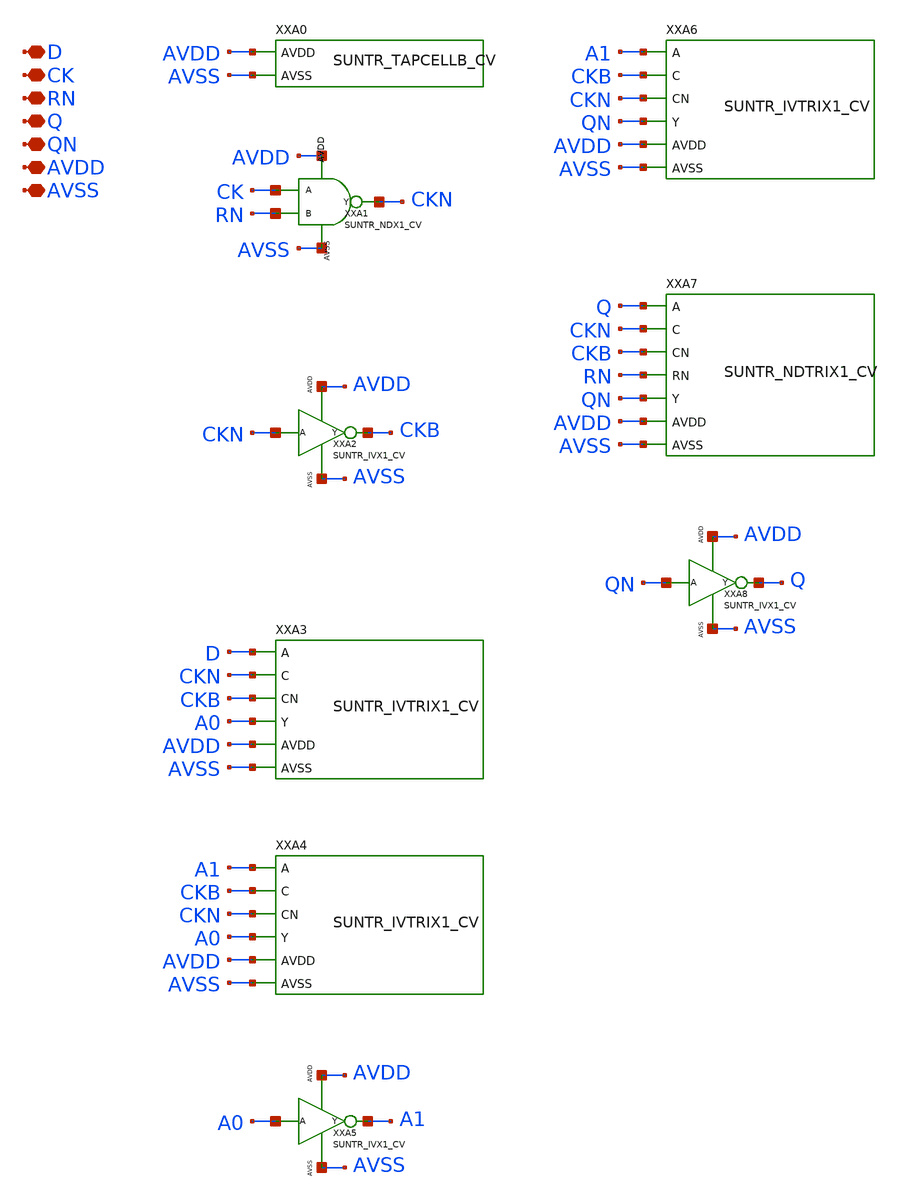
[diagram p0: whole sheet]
** sch_path: ip/sun_tr_sky130nm/design/SUN_TR_SKY130NM/SUNTR_DFRNQNX1_CV.sch
**.subckt SUNTR_DFRNQNX1_CV D CK RN Q QN AVDD AVSS
*.iopin D
*.iopin CK
*.iopin RN
*.iopin Q
*.iopin QN
*.iopin AVDD
*.iopin AVSS
XXA0 AVDD AVSS SUNTR_TAPCELLB_CV
XXA1 CK RN CKN AVDD AVSS SUNTR_NDX1_CV xoffset=0 yoffset=0 angle=0 M=1
XXA2 CKN CKB AVDD AVSS SUNTR_IVX1_CV
XXA3 D CKN CKB A0 AVDD AVSS SUNTR_IVTRIX1_CV xoffset=0 yoffset=0 angle=0 M=1
XXA4 A1 CKB CKN A0 AVDD AVSS SUNTR_IVTRIX1_CV xoffset=0 yoffset=0 angle=0 M=1
XXA5 A0 A1 AVDD AVSS SUNTR_IVX1_CV
XXA6 A1 CKB CKN QN AVDD AVSS SUNTR_IVTRIX1_CV xoffset=0 yoffset=0 angle=0 M=1
XXA7 Q CKN CKB RN QN AVDD AVSS SUNTR_NDTRIX1_CV xoffset=0 yoffset=0 angle=0 M=1
XXA8 QN Q AVDD AVSS SUNTR_IVX1_CV
**.ends
.end
